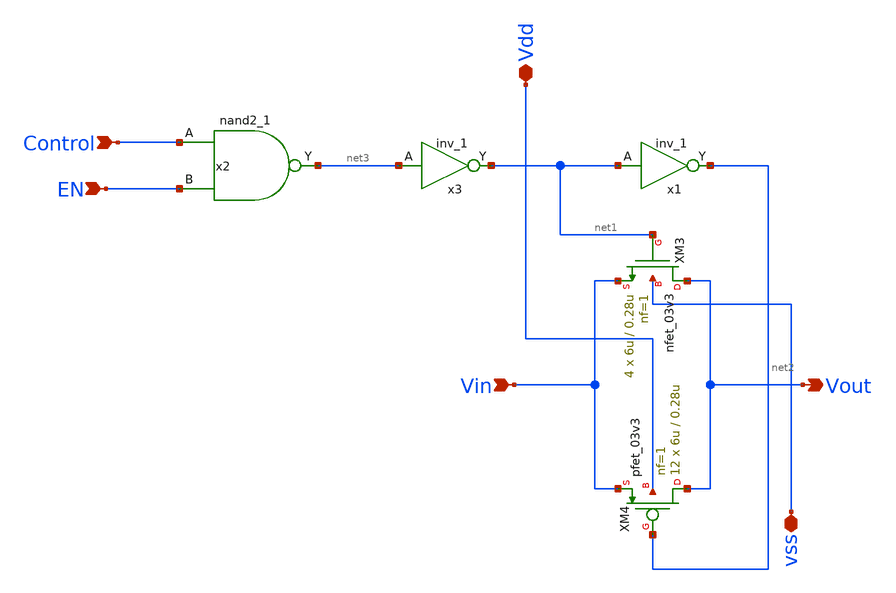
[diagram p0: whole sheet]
** sch_path: designs/libs/core_analog/tx_gate/transmission_gate_2.sch
**.subckt transmission_gate_2 Vdd Control Vout Vin vss EN
*.iopin Vdd
*.ipin Control
*.opin Vout
*.ipin Vin
*.iopin vss
*.ipin EN
XM3 Vout net1 Vin vss nfet_03v3 L=0.28u W=6u nf=1 ad='int((nf+1)/2) * W/nf * 0.18u' as='int((nf+2)/2) * W/nf * 0.18u'
+ pd='2*int((nf+1)/2) * (W/nf + 0.18u)' ps='2*int((nf+2)/2) * (W/nf + 0.18u)' nrd='0.18u / W' nrs='0.18u / W'
+ sa=0 sb=0 sd=0 m=4
XM4 Vout net2 Vin Vdd pfet_03v3 L=0.28u W=6u nf=1 ad='int((nf+1)/2) * W/nf * 0.18u' as='int((nf+2)/2) * W/nf * 0.18u'
+ pd='2*int((nf+1)/2) * (W/nf + 0.18u)' ps='2*int((nf+2)/2) * (W/nf + 0.18u)' nrd='0.18u / W' nrs='0.18u / W'
+ sa=0 sb=0 sd=0 m=12
x1 net1 VSSd VDDd VSSd VDDd net2 gf180mcu_fd_sc_mcu9t5v0__inv_1
x2 Control EN VSSd VDDd VSSd VDDd net3 gf180mcu_fd_sc_mcu9t5v0__nand2_1
x3 net3 VSSd VDDd VSSd VDDd net1 gf180mcu_fd_sc_mcu9t5v0__inv_1
**.ends
.end
